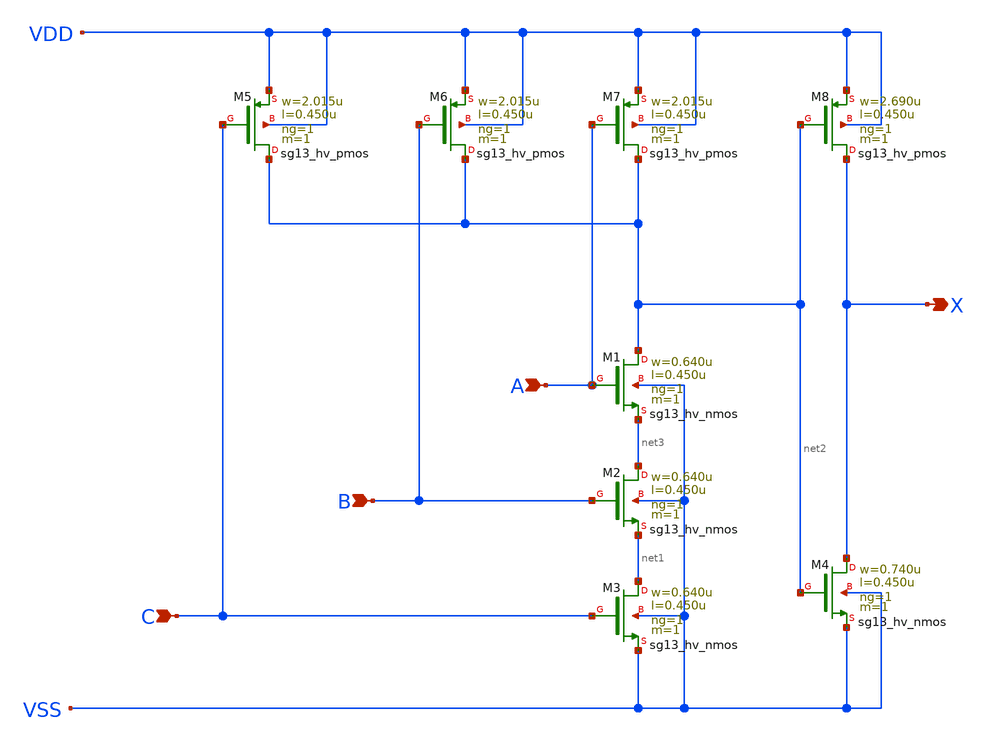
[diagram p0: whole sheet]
** sch_path: ihp-sg13g2/libs.ref/sg13g2_stdcell_hv/sch/xschem/sg13g2_hv_and3_1.sch
* Copyright 2023 IHP PDK Authors
* Licensed under the Apache License, Version 2.0 (the "License");
* you may not use this file except in compliance with the License.
* You may obtain a copy of the License at
* https://www.apache.org/licenses/LICENSE-2.0
* Unless required by applicable law or agreed to in writing, software
* distributed under the License is distributed on an "AS IS" BASIS,
* WITHOUT WARRANTIES OR CONDITIONS OF ANY KIND, either express or implied.
* See the License for the specific language governing permissions and
* limitations under the License.
**.subckt sg13g2_hv_and3_1 X C B A
*.opin X
*.ipin C
*.ipin B
*.ipin A
XM1 net2 A net3 VSS sg13_hv_nmos w=0.640u l=0.450u ng=1 m=1 mm_ok=1
XM2 net3 B net1 VSS sg13_hv_nmos w=0.640u l=0.450u ng=1 m=1 mm_ok=1
XM3 net1 C VSS VSS sg13_hv_nmos w=0.640u l=0.450u ng=1 m=1 mm_ok=1
XM4 X net2 VSS VSS sg13_hv_nmos w=0.740u l=0.450u ng=1 m=1 mm_ok=1
XM5 net2 C VDD VDD sg13_hv_pmos w=2.015u l=0.450u ng=1 m=1 mm_ok=1
XM6 net2 B VDD VDD sg13_hv_pmos w=2.015u l=0.450u ng=1 m=1 mm_ok=1
XM7 net2 A VDD VDD sg13_hv_pmos w=2.015u l=0.450u ng=1 m=1 mm_ok=1
XM8 X net2 VDD VDD sg13_hv_pmos w=2.690u l=0.450u ng=1 m=1 mm_ok=1
**.ends
.end
